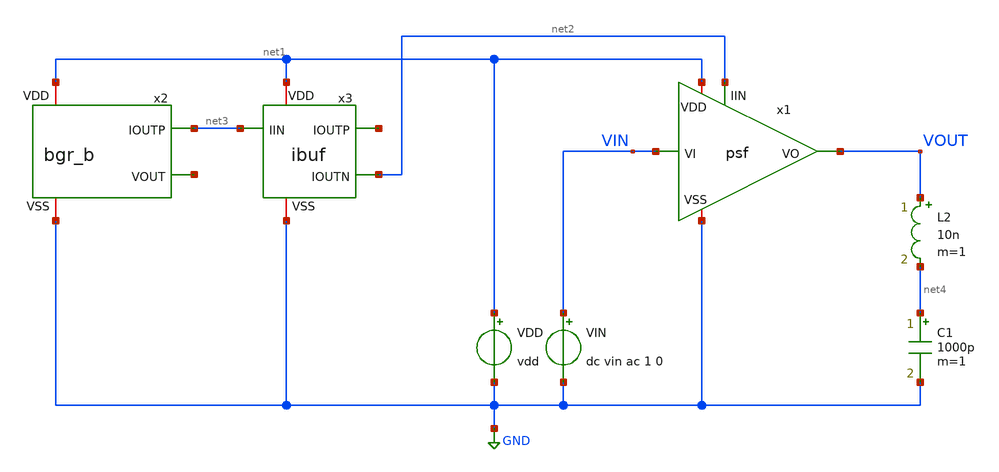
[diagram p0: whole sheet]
** sch_path: member_project/BGR/Maehashi/design/tb_psf.sch
**.subckt tb_psf
VDD net1 GND vdd
VIN VIN GND dc vin ac 1 0
C1 net4 GND 1000p m=1
x2 net1 net3 net5 GND bgr_b
x3 net1 net6 net3 net2 GND ibuf
x1 net1 VIN VOUT net2 GND psf
L2 VOUT net4 10n m=1
**** begin user architecture code


.option savecurrents
.temp 80
.param vdd = 4.5
.param vin = vdd/2
.control
set units=degree
save all

alterparam vthMN = 0.1 ; Slow:0.1, Fast:-0.1
alterparam vthMP = -0.1 ; Slow:-0.1, Fast:0.1
alterparam magRS = 1.2 ; Slow:1.2, Fast:0.85
reset

op
show m

dc VIN 0 4.5 0.1
plot v(VIN) v(VOUT)
plot v(VOUT) - v(VIN)


.endc

 .include $::LIB/ip62_models
**** end user architecture code
**.ends
.GLOBAL GND
.end
